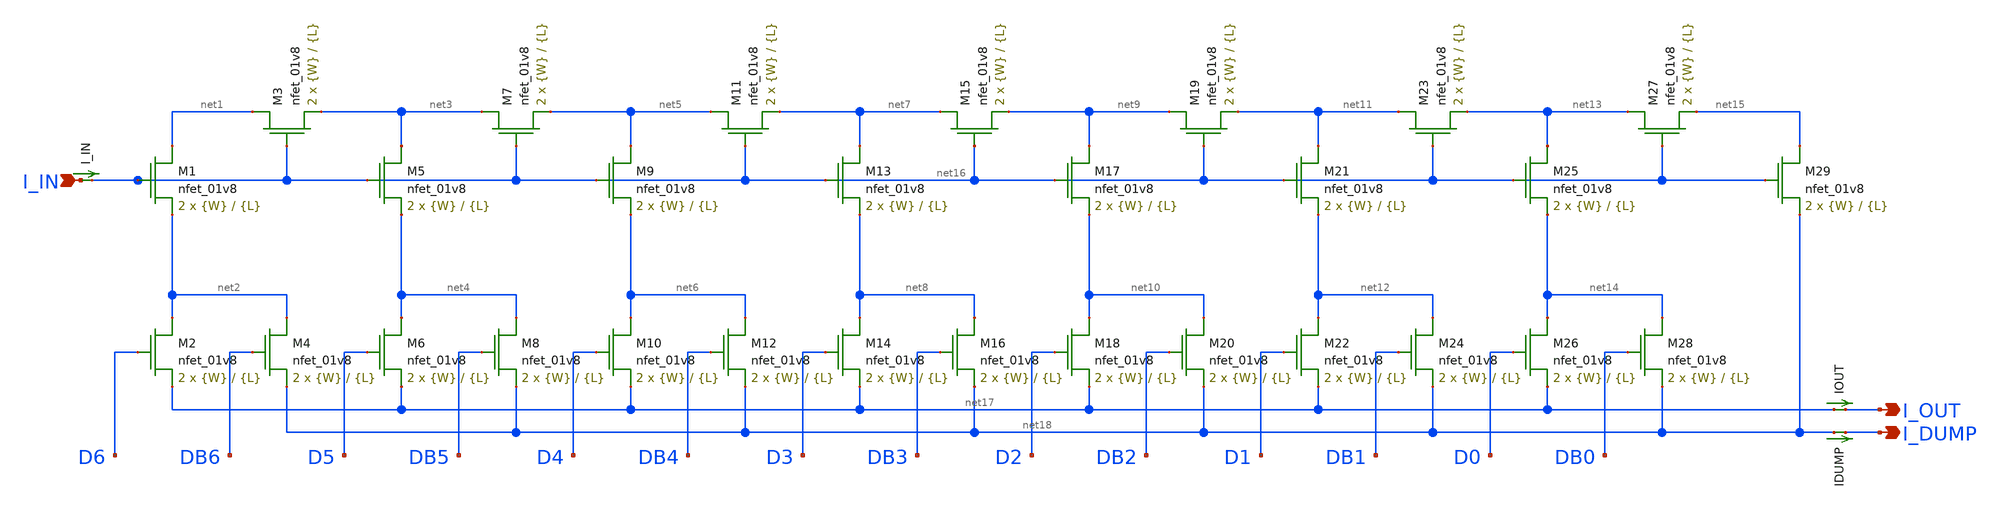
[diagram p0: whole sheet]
** sch_path: schemas/M2M_ladder.sch
**.subckt M2M_ladder I_OUT I_DUMP I_IN
*.opin I_OUT
*.opin I_DUMP
*.ipin I_IN
XM1 net1 net16 net2 GND sky130_fd_pr__nfet_01v8 L={L} W={W} nf=1 ad='int((nf+1)/2) * W/nf * 0.29' as='int((nf+2)/2) * W/nf * 0.29'
+ pd='2*int((nf+1)/2) * (W/nf + 0.29)' ps='2*int((nf+2)/2) * (W/nf + 0.29)' nrd='0.29 / W' nrs='0.29 / W'
+ sa=0 sb=0 sd=0 mult=2 m=2
IOUT net17 I_OUT 0
.save i(iout)
XM2 net2 D6 net17 GND sky130_fd_pr__nfet_01v8 L={L} W={W} nf=1 ad='int((nf+1)/2) * W/nf * 0.29' as='int((nf+2)/2) * W/nf * 0.29'
+ pd='2*int((nf+1)/2) * (W/nf + 0.29)' ps='2*int((nf+2)/2) * (W/nf + 0.29)' nrd='0.29 / W' nrs='0.29 / W'
+ sa=0 sb=0 sd=0 mult=2 m=2
XM3 net1 net16 net3 GND sky130_fd_pr__nfet_01v8 L={L} W={W} nf=1 ad='int((nf+1)/2) * W/nf * 0.29' as='int((nf+2)/2) * W/nf * 0.29'
+ pd='2*int((nf+1)/2) * (W/nf + 0.29)' ps='2*int((nf+2)/2) * (W/nf + 0.29)' nrd='0.29 / W' nrs='0.29 / W'
+ sa=0 sb=0 sd=0 mult=2 m=2
XM4 net2 DB6 net18 GND sky130_fd_pr__nfet_01v8 L={L} W={W} nf=1 ad='int((nf+1)/2) * W/nf * 0.29' as='int((nf+2)/2) * W/nf * 0.29'
+ pd='2*int((nf+1)/2) * (W/nf + 0.29)' ps='2*int((nf+2)/2) * (W/nf + 0.29)' nrd='0.29 / W' nrs='0.29 / W'
+ sa=0 sb=0 sd=0 mult=2 m=2
XM5 net3 net16 net4 GND sky130_fd_pr__nfet_01v8 L={L} W={W} nf=1 ad='int((nf+1)/2) * W/nf * 0.29' as='int((nf+2)/2) * W/nf * 0.29'
+ pd='2*int((nf+1)/2) * (W/nf + 0.29)' ps='2*int((nf+2)/2) * (W/nf + 0.29)' nrd='0.29 / W' nrs='0.29 / W'
+ sa=0 sb=0 sd=0 mult=2 m=2
XM6 net4 D5 net17 GND sky130_fd_pr__nfet_01v8 L={L} W={W} nf=1 ad='int((nf+1)/2) * W/nf * 0.29' as='int((nf+2)/2) * W/nf * 0.29'
+ pd='2*int((nf+1)/2) * (W/nf + 0.29)' ps='2*int((nf+2)/2) * (W/nf + 0.29)' nrd='0.29 / W' nrs='0.29 / W'
+ sa=0 sb=0 sd=0 mult=2 m=2
XM7 net3 net16 net5 GND sky130_fd_pr__nfet_01v8 L={L} W={W} nf=1 ad='int((nf+1)/2) * W/nf * 0.29' as='int((nf+2)/2) * W/nf * 0.29'
+ pd='2*int((nf+1)/2) * (W/nf + 0.29)' ps='2*int((nf+2)/2) * (W/nf + 0.29)' nrd='0.29 / W' nrs='0.29 / W'
+ sa=0 sb=0 sd=0 mult=2 m=2
XM8 net4 DB5 net18 GND sky130_fd_pr__nfet_01v8 L={L} W={W} nf=1 ad='int((nf+1)/2) * W/nf * 0.29' as='int((nf+2)/2) * W/nf * 0.29'
+ pd='2*int((nf+1)/2) * (W/nf + 0.29)' ps='2*int((nf+2)/2) * (W/nf + 0.29)' nrd='0.29 / W' nrs='0.29 / W'
+ sa=0 sb=0 sd=0 mult=2 m=2
XM9 net5 net16 net6 GND sky130_fd_pr__nfet_01v8 L={L} W={W} nf=1 ad='int((nf+1)/2) * W/nf * 0.29' as='int((nf+2)/2) * W/nf * 0.29'
+ pd='2*int((nf+1)/2) * (W/nf + 0.29)' ps='2*int((nf+2)/2) * (W/nf + 0.29)' nrd='0.29 / W' nrs='0.29 / W'
+ sa=0 sb=0 sd=0 mult=2 m=2
XM10 net6 D4 net17 GND sky130_fd_pr__nfet_01v8 L={L} W={W} nf=1 ad='int((nf+1)/2) * W/nf * 0.29' as='int((nf+2)/2) * W/nf * 0.29'
+ pd='2*int((nf+1)/2) * (W/nf + 0.29)' ps='2*int((nf+2)/2) * (W/nf + 0.29)' nrd='0.29 / W' nrs='0.29 / W'
+ sa=0 sb=0 sd=0 mult=2 m=2
XM11 net5 net16 net7 GND sky130_fd_pr__nfet_01v8 L={L} W={W} nf=1 ad='int((nf+1)/2) * W/nf * 0.29' as='int((nf+2)/2) * W/nf * 0.29'
+ pd='2*int((nf+1)/2) * (W/nf + 0.29)' ps='2*int((nf+2)/2) * (W/nf + 0.29)' nrd='0.29 / W' nrs='0.29 / W'
+ sa=0 sb=0 sd=0 mult=2 m=2
XM12 net6 DB4 net18 GND sky130_fd_pr__nfet_01v8 L={L} W={W} nf=1 ad='int((nf+1)/2) * W/nf * 0.29' as='int((nf+2)/2) * W/nf * 0.29'
+ pd='2*int((nf+1)/2) * (W/nf + 0.29)' ps='2*int((nf+2)/2) * (W/nf + 0.29)' nrd='0.29 / W' nrs='0.29 / W'
+ sa=0 sb=0 sd=0 mult=2 m=2
XM13 net7 net16 net8 GND sky130_fd_pr__nfet_01v8 L={L} W={W} nf=1 ad='int((nf+1)/2) * W/nf * 0.29' as='int((nf+2)/2) * W/nf * 0.29'
+ pd='2*int((nf+1)/2) * (W/nf + 0.29)' ps='2*int((nf+2)/2) * (W/nf + 0.29)' nrd='0.29 / W' nrs='0.29 / W'
+ sa=0 sb=0 sd=0 mult=2 m=2
XM14 net8 D3 net17 GND sky130_fd_pr__nfet_01v8 L={L} W={W} nf=1 ad='int((nf+1)/2) * W/nf * 0.29' as='int((nf+2)/2) * W/nf * 0.29'
+ pd='2*int((nf+1)/2) * (W/nf + 0.29)' ps='2*int((nf+2)/2) * (W/nf + 0.29)' nrd='0.29 / W' nrs='0.29 / W'
+ sa=0 sb=0 sd=0 mult=2 m=2
XM15 net7 net16 net9 GND sky130_fd_pr__nfet_01v8 L={L} W={W} nf=1 ad='int((nf+1)/2) * W/nf * 0.29' as='int((nf+2)/2) * W/nf * 0.29'
+ pd='2*int((nf+1)/2) * (W/nf + 0.29)' ps='2*int((nf+2)/2) * (W/nf + 0.29)' nrd='0.29 / W' nrs='0.29 / W'
+ sa=0 sb=0 sd=0 mult=2 m=2
XM16 net8 DB3 net18 GND sky130_fd_pr__nfet_01v8 L={L} W={W} nf=1 ad='int((nf+1)/2) * W/nf * 0.29' as='int((nf+2)/2) * W/nf * 0.29'
+ pd='2*int((nf+1)/2) * (W/nf + 0.29)' ps='2*int((nf+2)/2) * (W/nf + 0.29)' nrd='0.29 / W' nrs='0.29 / W'
+ sa=0 sb=0 sd=0 mult=2 m=2
XM17 net9 net16 net10 GND sky130_fd_pr__nfet_01v8 L={L} W={W} nf=1 ad='int((nf+1)/2) * W/nf * 0.29' as='int((nf+2)/2) * W/nf * 0.29'
+ pd='2*int((nf+1)/2) * (W/nf + 0.29)' ps='2*int((nf+2)/2) * (W/nf + 0.29)' nrd='0.29 / W' nrs='0.29 / W'
+ sa=0 sb=0 sd=0 mult=2 m=2
XM18 net10 D2 net17 GND sky130_fd_pr__nfet_01v8 L={L} W={W} nf=1 ad='int((nf+1)/2) * W/nf * 0.29' as='int((nf+2)/2) * W/nf * 0.29'
+ pd='2*int((nf+1)/2) * (W/nf + 0.29)' ps='2*int((nf+2)/2) * (W/nf + 0.29)' nrd='0.29 / W' nrs='0.29 / W'
+ sa=0 sb=0 sd=0 mult=2 m=2
XM19 net9 net16 net11 GND sky130_fd_pr__nfet_01v8 L={L} W={W} nf=1 ad='int((nf+1)/2) * W/nf * 0.29' as='int((nf+2)/2) * W/nf * 0.29'
+ pd='2*int((nf+1)/2) * (W/nf + 0.29)' ps='2*int((nf+2)/2) * (W/nf + 0.29)' nrd='0.29 / W' nrs='0.29 / W'
+ sa=0 sb=0 sd=0 mult=2 m=2
XM20 net10 DB2 net18 GND sky130_fd_pr__nfet_01v8 L={L} W={W} nf=1 ad='int((nf+1)/2) * W/nf * 0.29' as='int((nf+2)/2) * W/nf * 0.29'
+ pd='2*int((nf+1)/2) * (W/nf + 0.29)' ps='2*int((nf+2)/2) * (W/nf + 0.29)' nrd='0.29 / W' nrs='0.29 / W'
+ sa=0 sb=0 sd=0 mult=2 m=2
XM21 net11 net16 net12 GND sky130_fd_pr__nfet_01v8 L={L} W={W} nf=1 ad='int((nf+1)/2) * W/nf * 0.29'
+ as='int((nf+2)/2) * W/nf * 0.29' pd='2*int((nf+1)/2) * (W/nf + 0.29)' ps='2*int((nf+2)/2) * (W/nf + 0.29)'
+ nrd='0.29 / W' nrs='0.29 / W' sa=0 sb=0 sd=0 mult=2 m=2
XM22 net12 D1 net17 GND sky130_fd_pr__nfet_01v8 L={L} W={W} nf=1 ad='int((nf+1)/2) * W/nf * 0.29' as='int((nf+2)/2) * W/nf * 0.29'
+ pd='2*int((nf+1)/2) * (W/nf + 0.29)' ps='2*int((nf+2)/2) * (W/nf + 0.29)' nrd='0.29 / W' nrs='0.29 / W'
+ sa=0 sb=0 sd=0 mult=2 m=2
XM23 net11 net16 net13 GND sky130_fd_pr__nfet_01v8 L={L} W={W} nf=1 ad='int((nf+1)/2) * W/nf * 0.29'
+ as='int((nf+2)/2) * W/nf * 0.29' pd='2*int((nf+1)/2) * (W/nf + 0.29)' ps='2*int((nf+2)/2) * (W/nf + 0.29)'
+ nrd='0.29 / W' nrs='0.29 / W' sa=0 sb=0 sd=0 mult=2 m=2
XM24 net12 DB1 net18 GND sky130_fd_pr__nfet_01v8 L={L} W={W} nf=1 ad='int((nf+1)/2) * W/nf * 0.29' as='int((nf+2)/2) * W/nf * 0.29'
+ pd='2*int((nf+1)/2) * (W/nf + 0.29)' ps='2*int((nf+2)/2) * (W/nf + 0.29)' nrd='0.29 / W' nrs='0.29 / W'
+ sa=0 sb=0 sd=0 mult=2 m=2
XM25 net13 net16 net14 GND sky130_fd_pr__nfet_01v8 L={L} W={W} nf=1 ad='int((nf+1)/2) * W/nf * 0.29'
+ as='int((nf+2)/2) * W/nf * 0.29' pd='2*int((nf+1)/2) * (W/nf + 0.29)' ps='2*int((nf+2)/2) * (W/nf + 0.29)'
+ nrd='0.29 / W' nrs='0.29 / W' sa=0 sb=0 sd=0 mult=2 m=2
XM26 net14 D0 net17 GND sky130_fd_pr__nfet_01v8 L={L} W={W} nf=1 ad='int((nf+1)/2) * W/nf * 0.29' as='int((nf+2)/2) * W/nf * 0.29'
+ pd='2*int((nf+1)/2) * (W/nf + 0.29)' ps='2*int((nf+2)/2) * (W/nf + 0.29)' nrd='0.29 / W' nrs='0.29 / W'
+ sa=0 sb=0 sd=0 mult=2 m=2
XM27 net13 net16 net15 GND sky130_fd_pr__nfet_01v8 L={L} W={W} nf=1 ad='int((nf+1)/2) * W/nf * 0.29'
+ as='int((nf+2)/2) * W/nf * 0.29' pd='2*int((nf+1)/2) * (W/nf + 0.29)' ps='2*int((nf+2)/2) * (W/nf + 0.29)'
+ nrd='0.29 / W' nrs='0.29 / W' sa=0 sb=0 sd=0 mult=2 m=2
XM28 net14 DB0 net18 GND sky130_fd_pr__nfet_01v8 L={L} W={W} nf=1 ad='int((nf+1)/2) * W/nf * 0.29' as='int((nf+2)/2) * W/nf * 0.29'
+ pd='2*int((nf+1)/2) * (W/nf + 0.29)' ps='2*int((nf+2)/2) * (W/nf + 0.29)' nrd='0.29 / W' nrs='0.29 / W'
+ sa=0 sb=0 sd=0 mult=2 m=2
XM29 net15 net16 net18 GND sky130_fd_pr__nfet_01v8 L={L} W={W} nf=1 ad='int((nf+1)/2) * W/nf * 0.29'
+ as='int((nf+2)/2) * W/nf * 0.29' pd='2*int((nf+1)/2) * (W/nf + 0.29)' ps='2*int((nf+2)/2) * (W/nf + 0.29)'
+ nrd='0.29 / W' nrs='0.29 / W' sa=0 sb=0 sd=0 mult=2 m=2
IDUMP net18 I_DUMP 0
.save i(idump)
I_IN I_IN net16 0
.save i(i_in)
**.ends
.end
